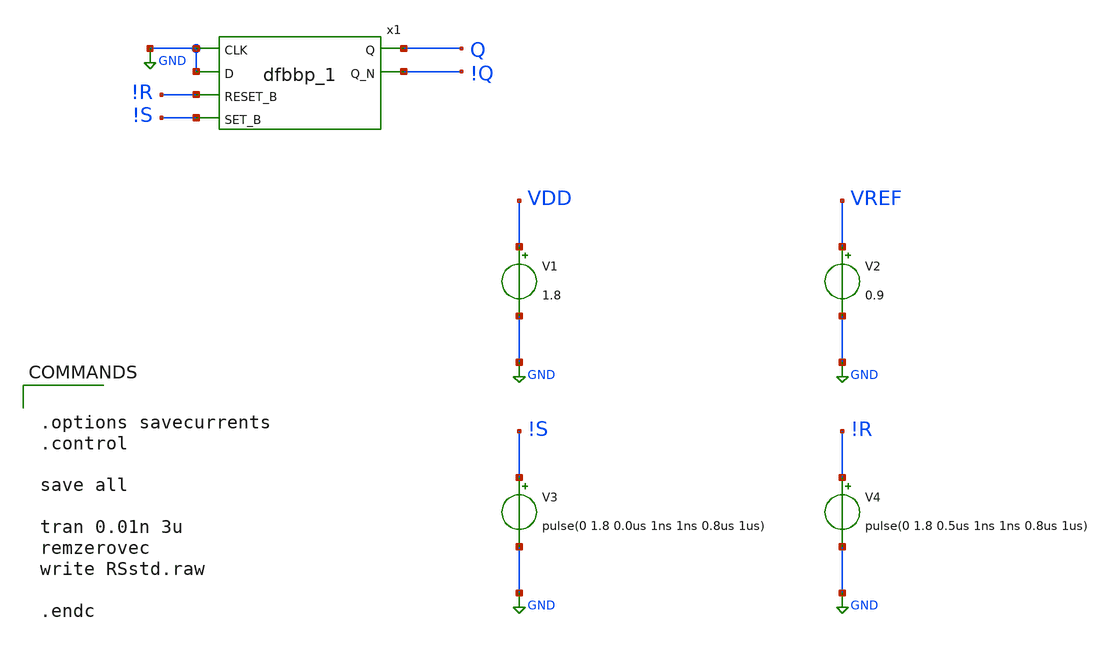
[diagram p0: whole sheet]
** sch_path: RSlatch/RSstd.sch
.lib $::SKYWATER_MODELS/sky130.lib.spice tt
.include $::SKYWATER_STDCELLS/sky130_fd_sc_hd.spice

**.subckt RSstd
V1 VDD GND 1.8
V2 VREF GND 0.9
V4 !R GND pulse(0 1.8 0.5us 1ns 1ns 0.8us 1us)
V3 !S GND pulse(0 1.8 0.0us 1ns 1ns 0.8us 1us)
x1 GND GND !R !S GND GND VDD VDD Q !Q sky130_fd_sc_hd__dfbbp_1
**** begin user architecture code


.options savecurrents
.control

save all

tran 0.01n 3u
remzerovec
write RSstd.raw

.endc


**** end user architecture code
**.ends
.GLOBAL GND
.end
